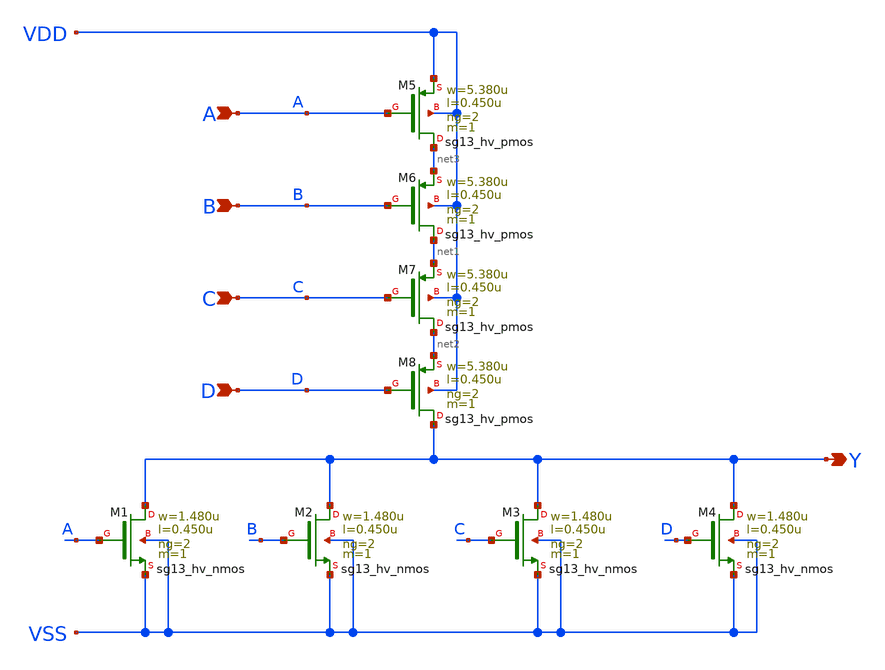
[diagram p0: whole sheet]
** sch_path: ihp-sg13g2/libs.ref/sg13g2_stdcell_hv/sch/xschem/sg13g2_hv_nor4_2.sch
* Copyright 2023 IHP PDK Authors
* Licensed under the Apache License, Version 2.0 (the "License");
* you may not use this file except in compliance with the License.
* You may obtain a copy of the License at
* https://www.apache.org/licenses/LICENSE-2.0
* Unless required by applicable law or agreed to in writing, software
* distributed under the License is distributed on an "AS IS" BASIS,
* WITHOUT WARRANTIES OR CONDITIONS OF ANY KIND, either express or implied.
* See the License for the specific language governing permissions and
* limitations under the License.
**.subckt sg13g2_hv_nor4_2 Y A B C D
*.opin Y
*.ipin A
*.ipin B
*.ipin C
*.ipin D
XM1 Y A VSS VSS sg13_hv_nmos w=1.480u l=0.450u ng=2 m=1 mm_ok=1
XM2 Y B VSS VSS sg13_hv_nmos w=1.480u l=0.450u ng=2 m=1 mm_ok=1
XM3 Y C VSS VSS sg13_hv_nmos w=1.480u l=0.450u ng=2 m=1 mm_ok=1
XM4 Y D VSS VSS sg13_hv_nmos w=1.480u l=0.450u ng=2 m=1 mm_ok=1
XM5 net3 A VDD VDD sg13_hv_pmos w=5.380u l=0.450u ng=2 m=1 mm_ok=1
XM6 net1 B net3 VDD sg13_hv_pmos w=5.380u l=0.450u ng=2 m=1 mm_ok=1
XM7 net2 C net1 VDD sg13_hv_pmos w=5.380u l=0.450u ng=2 m=1 mm_ok=1
XM8 Y D net2 VDD sg13_hv_pmos w=5.380u l=0.450u ng=2 m=1 mm_ok=1
**.ends
.end
